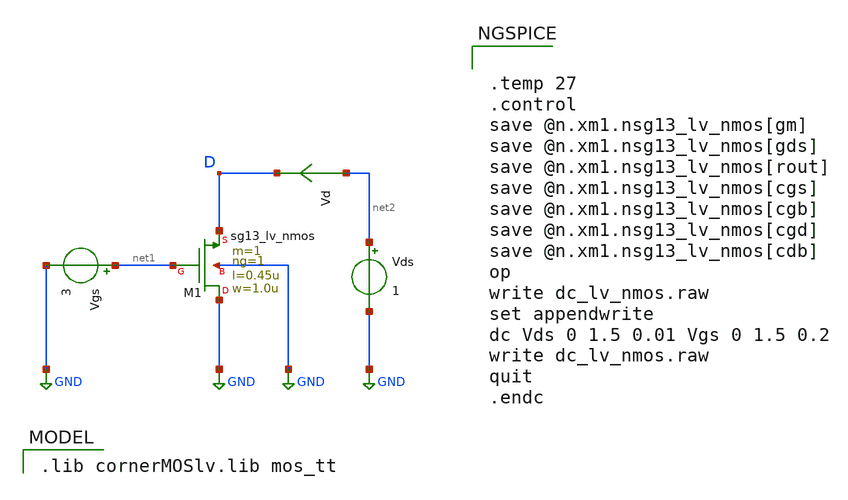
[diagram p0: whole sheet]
** sch_path: Single_MOS/lv_nmos.sch
**.subckt lv_nmos
XM1 GND net1 D GND sg13_lv_nmos w=1.0u l=0.45u ng=1 m=1 mm_ok=1
Vgs net1 GND 3
Vds net2 GND 1
.save i(vds)
Vd net2 D 0
.save i(vd)
**** begin user architecture code
 .lib cornerMOSlv.lib mos_tt



.temp 27
.control
save @n.xm1.nsg13_lv_nmos[gm]
save @n.xm1.nsg13_lv_nmos[gds]
save @n.xm1.nsg13_lv_nmos[rout]
save @n.xm1.nsg13_lv_nmos[cgs]
save @n.xm1.nsg13_lv_nmos[cgb]
save @n.xm1.nsg13_lv_nmos[cgd]
save @n.xm1.nsg13_lv_nmos[cdb]
op
write dc_lv_nmos.raw
set appendwrite
dc Vds 0 1.5 0.01 Vgs 0 1.5 0.2
write dc_lv_nmos.raw
quit
.endc


**** end user architecture code
**.ends
.GLOBAL GND
.end
